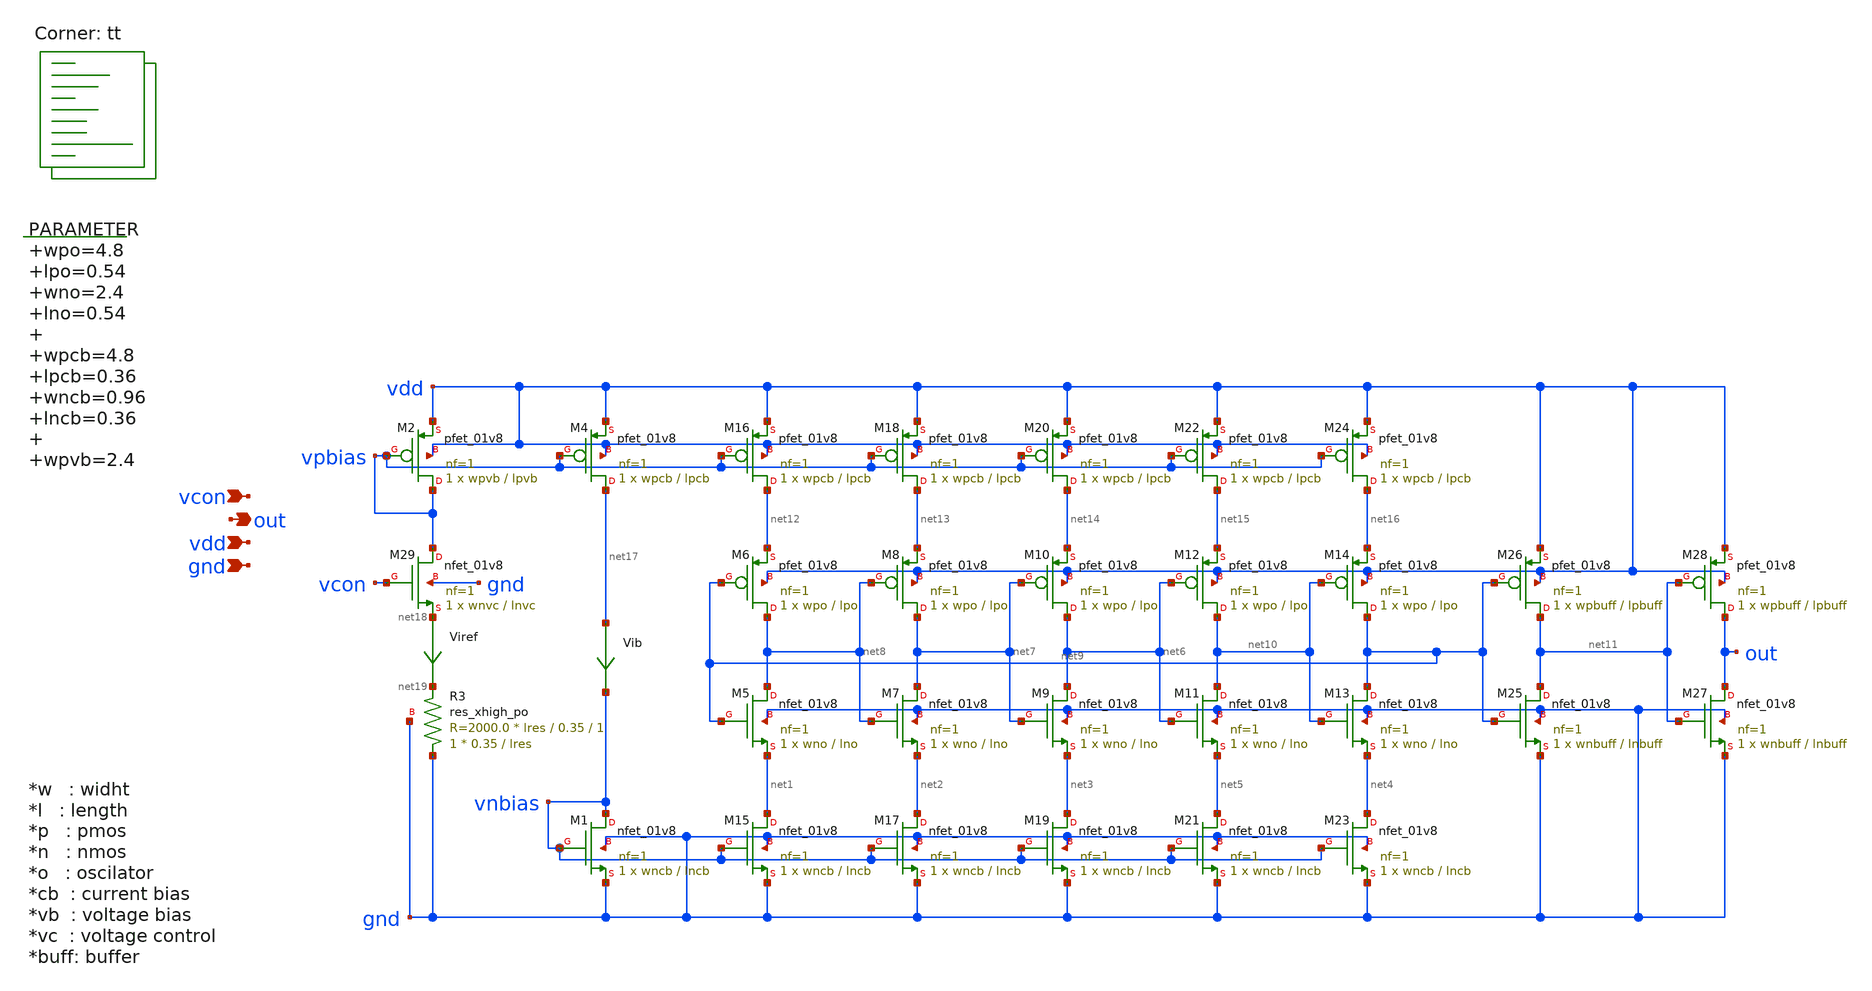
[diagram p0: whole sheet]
** sch_path: xschem/vco.sch
**.subckt vco vcon out vdd gnd
*.ipin vcon
*.opin out
*.ipin vdd
*.ipin gnd
.param wpo=4.8 lpo=0.54 wno=2.4 lno=0.54 wpcb=4.8 lpcb=0.36 wncb=0.96 lncb=0.36 wpvb=2.4 lpvb=0.36
+ wnvc=96 lnvc=0.9 wpbuff=4.8 lpbuff=0.18 wnbuff=1.2 lnbuff=0.18 rin=100 rex=10k lres=3.5

XM1 vnbias vnbias gnd gnd sky130_fd_pr__nfet_01v8 L=lncb W=wncb nf=1 ad='int((nf+1)/2) * W/nf * 0.29'
+ as='int((nf+2)/2) * W/nf * 0.29' pd='2*int((nf+1)/2) * (W/nf + 0.29)' ps='2*int((nf+2)/2) * (W/nf + 0.29)'
+ nrd='0.29 / W' nrs='0.29 / W' sa=0 sb=0 sd=0 mult=1 m=1
XM2 vpbias vpbias vdd vdd sky130_fd_pr__pfet_01v8 L=lpvb W=wpvb nf=1 ad='int((nf+1)/2) * W/nf * 0.29'
+ as='int((nf+2)/2) * W/nf * 0.29' pd='2*int((nf+1)/2) * (W/nf + 0.29)' ps='2*int((nf+2)/2) * (W/nf + 0.29)'
+ nrd='0.29 / W' nrs='0.29 / W' sa=0 sb=0 sd=0 mult=1 m=1
XM4 net17 vpbias vdd vdd sky130_fd_pr__pfet_01v8 L=lpcb W=wpcb nf=1 ad='int((nf+1)/2) * W/nf * 0.29'
+ as='int((nf+2)/2) * W/nf * 0.29' pd='2*int((nf+1)/2) * (W/nf + 0.29)' ps='2*int((nf+2)/2) * (W/nf + 0.29)'
+ nrd='0.29 / W' nrs='0.29 / W' sa=0 sb=0 sd=0 mult=1 m=1
XM5 net8 net9 net1 gnd sky130_fd_pr__nfet_01v8 L=lno W=wno nf=1 ad='int((nf+1)/2) * W/nf * 0.29' as='int((nf+2)/2) * W/nf * 0.29'
+ pd='2*int((nf+1)/2) * (W/nf + 0.29)' ps='2*int((nf+2)/2) * (W/nf + 0.29)' nrd='0.29 / W' nrs='0.29 / W'
+ sa=0 sb=0 sd=0 mult=1 m=1
XM6 net8 net9 net12 vdd sky130_fd_pr__pfet_01v8 L=lpo W=wpo nf=1 ad='int((nf+1)/2) * W/nf * 0.29' as='int((nf+2)/2) * W/nf * 0.29'
+ pd='2*int((nf+1)/2) * (W/nf + 0.29)' ps='2*int((nf+2)/2) * (W/nf + 0.29)' nrd='0.29 / W' nrs='0.29 / W'
+ sa=0 sb=0 sd=0 mult=1 m=1
XM7 net7 net8 net2 gnd sky130_fd_pr__nfet_01v8 L=lno W=wno nf=1 ad='int((nf+1)/2) * W/nf * 0.29' as='int((nf+2)/2) * W/nf * 0.29'
+ pd='2*int((nf+1)/2) * (W/nf + 0.29)' ps='2*int((nf+2)/2) * (W/nf + 0.29)' nrd='0.29 / W' nrs='0.29 / W'
+ sa=0 sb=0 sd=0 mult=1 m=1
XM8 net7 net8 net13 vdd sky130_fd_pr__pfet_01v8 L=lpo W=wpo nf=1 ad='int((nf+1)/2) * W/nf * 0.29' as='int((nf+2)/2) * W/nf * 0.29'
+ pd='2*int((nf+1)/2) * (W/nf + 0.29)' ps='2*int((nf+2)/2) * (W/nf + 0.29)' nrd='0.29 / W' nrs='0.29 / W'
+ sa=0 sb=0 sd=0 mult=1 m=1
XM9 net6 net7 net3 gnd sky130_fd_pr__nfet_01v8 L=lno W=wno nf=1 ad='int((nf+1)/2) * W/nf * 0.29' as='int((nf+2)/2) * W/nf * 0.29'
+ pd='2*int((nf+1)/2) * (W/nf + 0.29)' ps='2*int((nf+2)/2) * (W/nf + 0.29)' nrd='0.29 / W' nrs='0.29 / W'
+ sa=0 sb=0 sd=0 mult=1 m=1
XM10 net6 net7 net14 vdd sky130_fd_pr__pfet_01v8 L=lpo W=wpo nf=1 ad='int((nf+1)/2) * W/nf * 0.29' as='int((nf+2)/2) * W/nf * 0.29'
+ pd='2*int((nf+1)/2) * (W/nf + 0.29)' ps='2*int((nf+2)/2) * (W/nf + 0.29)' nrd='0.29 / W' nrs='0.29 / W'
+ sa=0 sb=0 sd=0 mult=1 m=1
XM11 net10 net6 net5 gnd sky130_fd_pr__nfet_01v8 L=lno W=wno nf=1 ad='int((nf+1)/2) * W/nf * 0.29' as='int((nf+2)/2) * W/nf * 0.29'
+ pd='2*int((nf+1)/2) * (W/nf + 0.29)' ps='2*int((nf+2)/2) * (W/nf + 0.29)' nrd='0.29 / W' nrs='0.29 / W'
+ sa=0 sb=0 sd=0 mult=1 m=1
XM12 net10 net6 net15 vdd sky130_fd_pr__pfet_01v8 L=lpo W=wpo nf=1 ad='int((nf+1)/2) * W/nf * 0.29' as='int((nf+2)/2) * W/nf * 0.29'
+ pd='2*int((nf+1)/2) * (W/nf + 0.29)' ps='2*int((nf+2)/2) * (W/nf + 0.29)' nrd='0.29 / W' nrs='0.29 / W'
+ sa=0 sb=0 sd=0 mult=1 m=1
XM13 net9 net10 net4 gnd sky130_fd_pr__nfet_01v8 L=lno W=wno nf=1 ad='int((nf+1)/2) * W/nf * 0.29' as='int((nf+2)/2) * W/nf * 0.29'
+ pd='2*int((nf+1)/2) * (W/nf + 0.29)' ps='2*int((nf+2)/2) * (W/nf + 0.29)' nrd='0.29 / W' nrs='0.29 / W'
+ sa=0 sb=0 sd=0 mult=1 m=1
XM14 net9 net10 net16 vdd sky130_fd_pr__pfet_01v8 L=lpo W=wpo nf=1 ad='int((nf+1)/2) * W/nf * 0.29' as='int((nf+2)/2) * W/nf * 0.29'
+ pd='2*int((nf+1)/2) * (W/nf + 0.29)' ps='2*int((nf+2)/2) * (W/nf + 0.29)' nrd='0.29 / W' nrs='0.29 / W'
+ sa=0 sb=0 sd=0 mult=1 m=1
XM16 net12 vpbias vdd vdd sky130_fd_pr__pfet_01v8 L=lpcb W=wpcb nf=1 ad='int((nf+1)/2) * W/nf * 0.29'
+ as='int((nf+2)/2) * W/nf * 0.29' pd='2*int((nf+1)/2) * (W/nf + 0.29)' ps='2*int((nf+2)/2) * (W/nf + 0.29)'
+ nrd='0.29 / W' nrs='0.29 / W' sa=0 sb=0 sd=0 mult=1 m=1
XM18 net13 vpbias vdd vdd sky130_fd_pr__pfet_01v8 L=lpcb W=wpcb nf=1 ad='int((nf+1)/2) * W/nf * 0.29'
+ as='int((nf+2)/2) * W/nf * 0.29' pd='2*int((nf+1)/2) * (W/nf + 0.29)' ps='2*int((nf+2)/2) * (W/nf + 0.29)'
+ nrd='0.29 / W' nrs='0.29 / W' sa=0 sb=0 sd=0 mult=1 m=1
XM20 net14 vpbias vdd vdd sky130_fd_pr__pfet_01v8 L=lpcb W=wpcb nf=1 ad='int((nf+1)/2) * W/nf * 0.29'
+ as='int((nf+2)/2) * W/nf * 0.29' pd='2*int((nf+1)/2) * (W/nf + 0.29)' ps='2*int((nf+2)/2) * (W/nf + 0.29)'
+ nrd='0.29 / W' nrs='0.29 / W' sa=0 sb=0 sd=0 mult=1 m=1
XM22 net15 vpbias vdd vdd sky130_fd_pr__pfet_01v8 L=lpcb W=wpcb nf=1 ad='int((nf+1)/2) * W/nf * 0.29'
+ as='int((nf+2)/2) * W/nf * 0.29' pd='2*int((nf+1)/2) * (W/nf + 0.29)' ps='2*int((nf+2)/2) * (W/nf + 0.29)'
+ nrd='0.29 / W' nrs='0.29 / W' sa=0 sb=0 sd=0 mult=1 m=1
XM24 net16 vpbias vdd vdd sky130_fd_pr__pfet_01v8 L=lpcb W=wpcb nf=1 ad='int((nf+1)/2) * W/nf * 0.29'
+ as='int((nf+2)/2) * W/nf * 0.29' pd='2*int((nf+1)/2) * (W/nf + 0.29)' ps='2*int((nf+2)/2) * (W/nf + 0.29)'
+ nrd='0.29 / W' nrs='0.29 / W' sa=0 sb=0 sd=0 mult=1 m=1
XM25 net11 net9 gnd gnd sky130_fd_pr__nfet_01v8 L=lnbuff W=wnbuff nf=1 ad='int((nf+1)/2) * W/nf * 0.29'
+ as='int((nf+2)/2) * W/nf * 0.29' pd='2*int((nf+1)/2) * (W/nf + 0.29)' ps='2*int((nf+2)/2) * (W/nf + 0.29)'
+ nrd='0.29 / W' nrs='0.29 / W' sa=0 sb=0 sd=0 mult=1 m=1
XM26 net11 net9 vdd vdd sky130_fd_pr__pfet_01v8 L=lpbuff W=wpbuff nf=1 ad='int((nf+1)/2) * W/nf * 0.29'
+ as='int((nf+2)/2) * W/nf * 0.29' pd='2*int((nf+1)/2) * (W/nf + 0.29)' ps='2*int((nf+2)/2) * (W/nf + 0.29)'
+ nrd='0.29 / W' nrs='0.29 / W' sa=0 sb=0 sd=0 mult=1 m=1
XM27 out net11 gnd gnd sky130_fd_pr__nfet_01v8 L=lnbuff W=wnbuff nf=1 ad='int((nf+1)/2) * W/nf * 0.29'
+ as='int((nf+2)/2) * W/nf * 0.29' pd='2*int((nf+1)/2) * (W/nf + 0.29)' ps='2*int((nf+2)/2) * (W/nf + 0.29)'
+ nrd='0.29 / W' nrs='0.29 / W' sa=0 sb=0 sd=0 mult=1 m=1
XM28 out net11 vdd vdd sky130_fd_pr__pfet_01v8 L=lpbuff W=wpbuff nf=1 ad='int((nf+1)/2) * W/nf * 0.29'
+ as='int((nf+2)/2) * W/nf * 0.29' pd='2*int((nf+1)/2) * (W/nf + 0.29)' ps='2*int((nf+2)/2) * (W/nf + 0.29)'
+ nrd='0.29 / W' nrs='0.29 / W' sa=0 sb=0 sd=0 mult=1 m=1
XM15 net1 vnbias gnd gnd sky130_fd_pr__nfet_01v8 L=lncb W=wncb nf=1 ad='int((nf+1)/2) * W/nf * 0.29'
+ as='int((nf+2)/2) * W/nf * 0.29' pd='2*int((nf+1)/2) * (W/nf + 0.29)' ps='2*int((nf+2)/2) * (W/nf + 0.29)'
+ nrd='0.29 / W' nrs='0.29 / W' sa=0 sb=0 sd=0 mult=1 m=1
XM17 net2 vnbias gnd gnd sky130_fd_pr__nfet_01v8 L=lncb W=wncb nf=1 ad='int((nf+1)/2) * W/nf * 0.29'
+ as='int((nf+2)/2) * W/nf * 0.29' pd='2*int((nf+1)/2) * (W/nf + 0.29)' ps='2*int((nf+2)/2) * (W/nf + 0.29)'
+ nrd='0.29 / W' nrs='0.29 / W' sa=0 sb=0 sd=0 mult=1 m=1
XM19 net3 vnbias gnd gnd sky130_fd_pr__nfet_01v8 L=lncb W=wncb nf=1 ad='int((nf+1)/2) * W/nf * 0.29'
+ as='int((nf+2)/2) * W/nf * 0.29' pd='2*int((nf+1)/2) * (W/nf + 0.29)' ps='2*int((nf+2)/2) * (W/nf + 0.29)'
+ nrd='0.29 / W' nrs='0.29 / W' sa=0 sb=0 sd=0 mult=1 m=1
XM21 net5 vnbias gnd gnd sky130_fd_pr__nfet_01v8 L=lncb W=wncb nf=1 ad='int((nf+1)/2) * W/nf * 0.29'
+ as='int((nf+2)/2) * W/nf * 0.29' pd='2*int((nf+1)/2) * (W/nf + 0.29)' ps='2*int((nf+2)/2) * (W/nf + 0.29)'
+ nrd='0.29 / W' nrs='0.29 / W' sa=0 sb=0 sd=0 mult=1 m=1
XM23 net4 vnbias gnd gnd sky130_fd_pr__nfet_01v8 L=lncb W=wncb nf=1 ad='int((nf+1)/2) * W/nf * 0.29'
+ as='int((nf+2)/2) * W/nf * 0.29' pd='2*int((nf+1)/2) * (W/nf + 0.29)' ps='2*int((nf+2)/2) * (W/nf + 0.29)'
+ nrd='0.29 / W' nrs='0.29 / W' sa=0 sb=0 sd=0 mult=1 m=1
Viref net18 net19 0
.save i(viref)
Vib net17 vnbias 0
.save i(vib)
XR3 gnd net19 gnd sky130_fd_pr__res_xhigh_po W=0.35 L=lres mult=1 m=1
XM29 vpbias vcon net18 gnd sky130_fd_pr__nfet_01v8 L=lnvc W=wnvc nf=1 ad='int((nf+1)/2) * W/nf * 0.29'
+ as='int((nf+2)/2) * W/nf * 0.29' pd='2*int((nf+1)/2) * (W/nf + 0.29)' ps='2*int((nf+2)/2) * (W/nf + 0.29)'
+ nrd='0.29 / W' nrs='0.29 / W' sa=0 sb=0 sd=0 mult=1 m=1
**** begin user architecture code
 .lib $::SKYWATER_MODELS/sky130.lib.spice tt

.param mc_mm_switch = 0
.param mc_pr_switch = 0




  .option wnflag=1
  .option safecurrents

  .param val=0.35
  .param lres=2.1

  Vvdd vdd  gnd dc 1.8
  Vcon vcon gnd dc 1.5

  .control
    reset
    save all
    write vco.raw
    set appendwrite
    let l_it = 0.35
    *while l_it <= 7.0
      alterparam lres = $&l_it
      reset
      save all
      tran 0.01n 150n
      write vco.raw
      let l_it = l_it + 0.35

      alterparam lres = $&l_it
      reset
      save all
      tran 0.01n 150n
      write vco.raw
      let l_it = l_it + 0.35

      alterparam lres = $&l_it
      reset
      save all
      tran 0.01n 150n
      write vco.raw
      let l_it = l_it + 0.35

      alterparam lres = $&l_it
      reset
      save all
      tran 0.01n 150n
      write vco.raw
      let l_it = l_it + 0.35

      alterparam lres = $&l_it
      reset
      save all
      tran 0.01n 150n
      write vco.raw
      let l_it = l_it + 0.35
    *end
    quit 0
  .endc



**** end user architecture code
**.ends
.end
